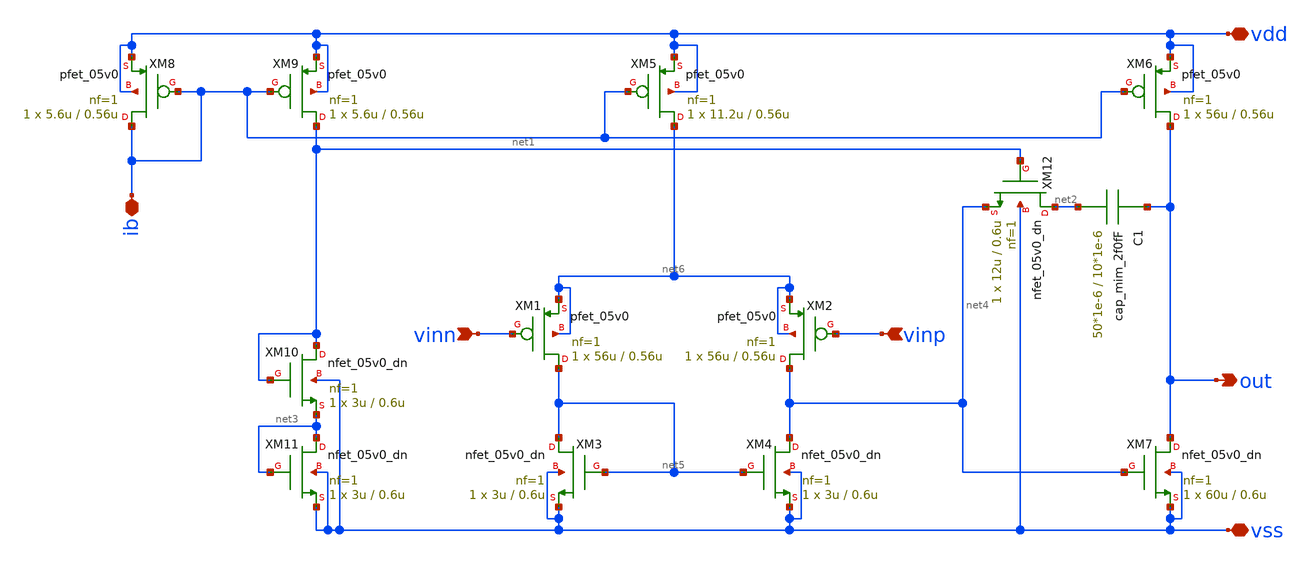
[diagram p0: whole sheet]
** sch_path: member_project/noritsuna/opamp/xschem/opamp.sch
**.subckt opamp vdd ib out vss vinn vinp
*.iopin vdd
*.iopin ib
*.opin out
*.iopin vss
*.ipin vinn
*.ipin vinp
C1 out net2 cap_mim_2f0fF W=50*1e-6 L=10*1e-6
XM9 net1 ib vdd vdd pfet_05v0 L=0.56u W=5.6u nf=1 ad='int((nf+1)/2) * W/nf * 0.18u' as='int((nf+2)/2) * W/nf * 0.18u'
+ pd='2*int((nf+1)/2) * (W/nf + 0.18u)' ps='2*int((nf+2)/2) * (W/nf + 0.18u)' nrd='0.18u / W' nrs='0.18u / W'
+ sa=0 sb=0 sd=0 m=1
XM8 ib ib vdd vdd pfet_05v0 L=0.56u W=5.6u nf=1 ad='int((nf+1)/2) * W/nf * 0.18u' as='int((nf+2)/2) * W/nf * 0.18u'
+ pd='2*int((nf+1)/2) * (W/nf + 0.18u)' ps='2*int((nf+2)/2) * (W/nf + 0.18u)' nrd='0.18u / W' nrs='0.18u / W'
+ sa=0 sb=0 sd=0 m=1
XM6 out ib vdd vdd pfet_05v0 L=0.56u W=56u nf=1 ad='int((nf+1)/2) * W/nf * 0.18u' as='int((nf+2)/2) * W/nf * 0.18u'
+ pd='2*int((nf+1)/2) * (W/nf + 0.18u)' ps='2*int((nf+2)/2) * (W/nf + 0.18u)' nrd='0.18u / W' nrs='0.18u / W'
+ sa=0 sb=0 sd=0 m=1
XM1 net5 vinn net6 net6 pfet_05v0 L=0.56u W=56u nf=1 ad='int((nf+1)/2) * W/nf * 0.18u' as='int((nf+2)/2) * W/nf * 0.18u'
+ pd='2*int((nf+1)/2) * (W/nf + 0.18u)' ps='2*int((nf+2)/2) * (W/nf + 0.18u)' nrd='0.18u / W' nrs='0.18u / W'
+ sa=0 sb=0 sd=0 m=1
XM2 net4 vinp net6 net6 pfet_05v0 L=0.56u W=56u nf=1 ad='int((nf+1)/2) * W/nf * 0.18u' as='int((nf+2)/2) * W/nf * 0.18u'
+ pd='2*int((nf+1)/2) * (W/nf + 0.18u)' ps='2*int((nf+2)/2) * (W/nf + 0.18u)' nrd='0.18u / W' nrs='0.18u / W'
+ sa=0 sb=0 sd=0 m=1
XM10 net1 net1 net3 vss nfet_05v0_dn L=0.6u W=3u nf=1 ad='int((nf+1)/2) * W/nf * 0.18u' as='int((nf+2)/2) * W/nf * 0.18u'
+ pd='2*int((nf+1)/2) * (W/nf + 0.18u)' ps='2*int((nf+2)/2) * (W/nf + 0.18u)' nrd='0.18u / W' nrs='0.18u / W'
+ sa=0 sb=0 sd=0 m=1
XM11 net3 net3 vss vss nfet_05v0_dn L=0.6u W=3u nf=1 ad='int((nf+1)/2) * W/nf * 0.18u' as='int((nf+2)/2) * W/nf * 0.18u'
+ pd='2*int((nf+1)/2) * (W/nf + 0.18u)' ps='2*int((nf+2)/2) * (W/nf + 0.18u)' nrd='0.18u / W' nrs='0.18u / W'
+ sa=0 sb=0 sd=0 m=1
XM3 net5 net5 vss vss nfet_05v0_dn L=0.6u W=3u nf=1 ad='int((nf+1)/2) * W/nf * 0.18u' as='int((nf+2)/2) * W/nf * 0.18u'
+ pd='2*int((nf+1)/2) * (W/nf + 0.18u)' ps='2*int((nf+2)/2) * (W/nf + 0.18u)' nrd='0.18u / W' nrs='0.18u / W'
+ sa=0 sb=0 sd=0 m=1
XM4 net4 net5 vss vss nfet_05v0_dn L=0.6u W=3u nf=1 ad='int((nf+1)/2) * W/nf * 0.18u' as='int((nf+2)/2) * W/nf * 0.18u'
+ pd='2*int((nf+1)/2) * (W/nf + 0.18u)' ps='2*int((nf+2)/2) * (W/nf + 0.18u)' nrd='0.18u / W' nrs='0.18u / W'
+ sa=0 sb=0 sd=0 m=1
XM7 out net4 vss vss nfet_05v0_dn L=0.6u W=60u nf=1 ad='int((nf+1)/2) * W/nf * 0.18u' as='int((nf+2)/2) * W/nf * 0.18u'
+ pd='2*int((nf+1)/2) * (W/nf + 0.18u)' ps='2*int((nf+2)/2) * (W/nf + 0.18u)' nrd='0.18u / W' nrs='0.18u / W'
+ sa=0 sb=0 sd=0 m=1
XM12 net2 net1 net4 vss nfet_05v0_dn L=0.6u W=12u nf=1 ad='int((nf+1)/2) * W/nf * 0.18u' as='int((nf+2)/2) * W/nf * 0.18u'
+ pd='2*int((nf+1)/2) * (W/nf + 0.18u)' ps='2*int((nf+2)/2) * (W/nf + 0.18u)' nrd='0.18u / W' nrs='0.18u / W'
+ sa=0 sb=0 sd=0 m=1
XM5 net6 ib vdd vdd pfet_05v0 L=0.56u W=11.2u nf=1 ad='int((nf+1)/2) * W/nf * 0.18u' as='int((nf+2)/2) * W/nf * 0.18u'
+ pd='2*int((nf+1)/2) * (W/nf + 0.18u)' ps='2*int((nf+2)/2) * (W/nf + 0.18u)' nrd='0.18u / W' nrs='0.18u / W'
+ sa=0 sb=0 sd=0 m=1
**.ends
.end
